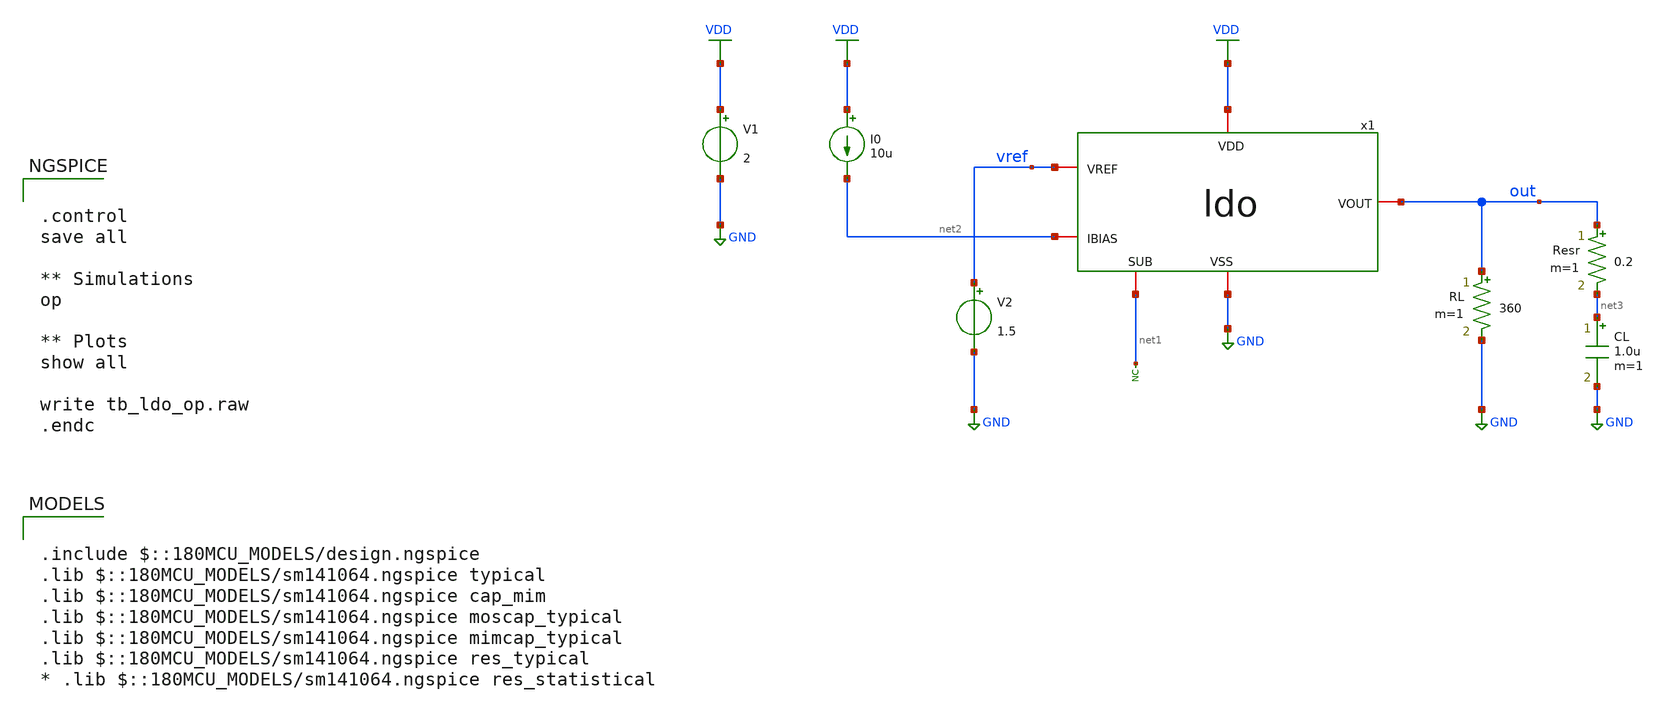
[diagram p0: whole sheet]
** sch_path: designs/libs/tb_ldo/tb_ldo/tb_ldo/tb_ldo_op/tb_ldo_op.sch
**.subckt tb_ldo_op
* noconn #net1
RL out GND 360 m=1
V1 VDD GND 2
V2 vref GND 1.5
I0 VDD net2 10u
CL net3 GND 1.0u m=1
Resr out net3 0.2 m=1
x1 VDD vref out net2 net1 GND ldo
**** begin user architecture code

.include $::180MCU_MODELS/design.ngspice
.lib $::180MCU_MODELS/sm141064.ngspice typical
.lib $::180MCU_MODELS/sm141064.ngspice cap_mim
.lib $::180MCU_MODELS/sm141064.ngspice moscap_typical
.lib $::180MCU_MODELS/sm141064.ngspice mimcap_typical
.lib $::180MCU_MODELS/sm141064.ngspice res_typical
* .lib $::180MCU_MODELS/sm141064.ngspice res_statistical



.control
save all

** Simulations
op

** Plots
show all

write tb_ldo_op.raw
.endc


**** end user architecture code
**.ends
.GLOBAL GND
.GLOBAL VDD
.end
